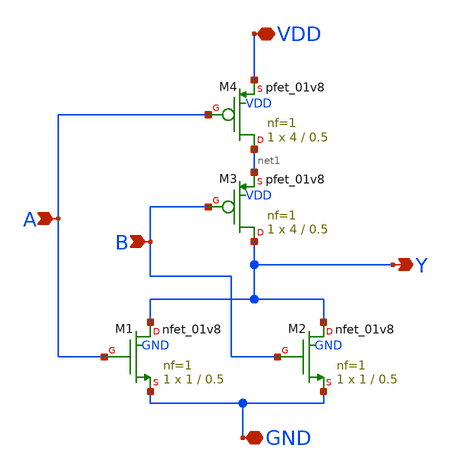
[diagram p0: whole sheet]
** sch_path: NOR/NOR.sch
**.subckt NOR A B GND VDD Y
*.ipin A
*.ipin B
*.iopin GND
*.iopin VDD
*.opin Y
XM1 Y A GND GND sky130_fd_pr__nfet_01v8 L=0.5 W=1 nf=1 ad='int((nf+1)/2) * W/nf * 0.29' as='int((nf+2)/2) * W/nf * 0.29'
+ pd='2*int((nf+1)/2) * (W/nf + 0.29)' ps='2*int((nf+2)/2) * (W/nf + 0.29)' nrd='0.29 / W' nrs='0.29 / W'
+ sa=0 sb=0 sd=0 mult=1 m=1
XM2 Y B GND GND sky130_fd_pr__nfet_01v8 L=0.5 W=1 nf=1 ad='int((nf+1)/2) * W/nf * 0.29' as='int((nf+2)/2) * W/nf * 0.29'
+ pd='2*int((nf+1)/2) * (W/nf + 0.29)' ps='2*int((nf+2)/2) * (W/nf + 0.29)' nrd='0.29 / W' nrs='0.29 / W'
+ sa=0 sb=0 sd=0 mult=1 m=1
XM3 Y B net1 VDD sky130_fd_pr__pfet_01v8 L=0.5 W=4 nf=1 ad='int((nf+1)/2) * W/nf * 0.29' as='int((nf+2)/2) * W/nf * 0.29'
+ pd='2*int((nf+1)/2) * (W/nf + 0.29)' ps='2*int((nf+2)/2) * (W/nf + 0.29)' nrd='0.29 / W' nrs='0.29 / W'
+ sa=0 sb=0 sd=0 mult=1 m=1
XM4 net1 A VDD VDD sky130_fd_pr__pfet_01v8 L=0.5 W=4 nf=1 ad='int((nf+1)/2) * W/nf * 0.29' as='int((nf+2)/2) * W/nf * 0.29'
+ pd='2*int((nf+1)/2) * (W/nf + 0.29)' ps='2*int((nf+2)/2) * (W/nf + 0.29)' nrd='0.29 / W' nrs='0.29 / W'
+ sa=0 sb=0 sd=0 mult=1 m=1
**.ends
.end
